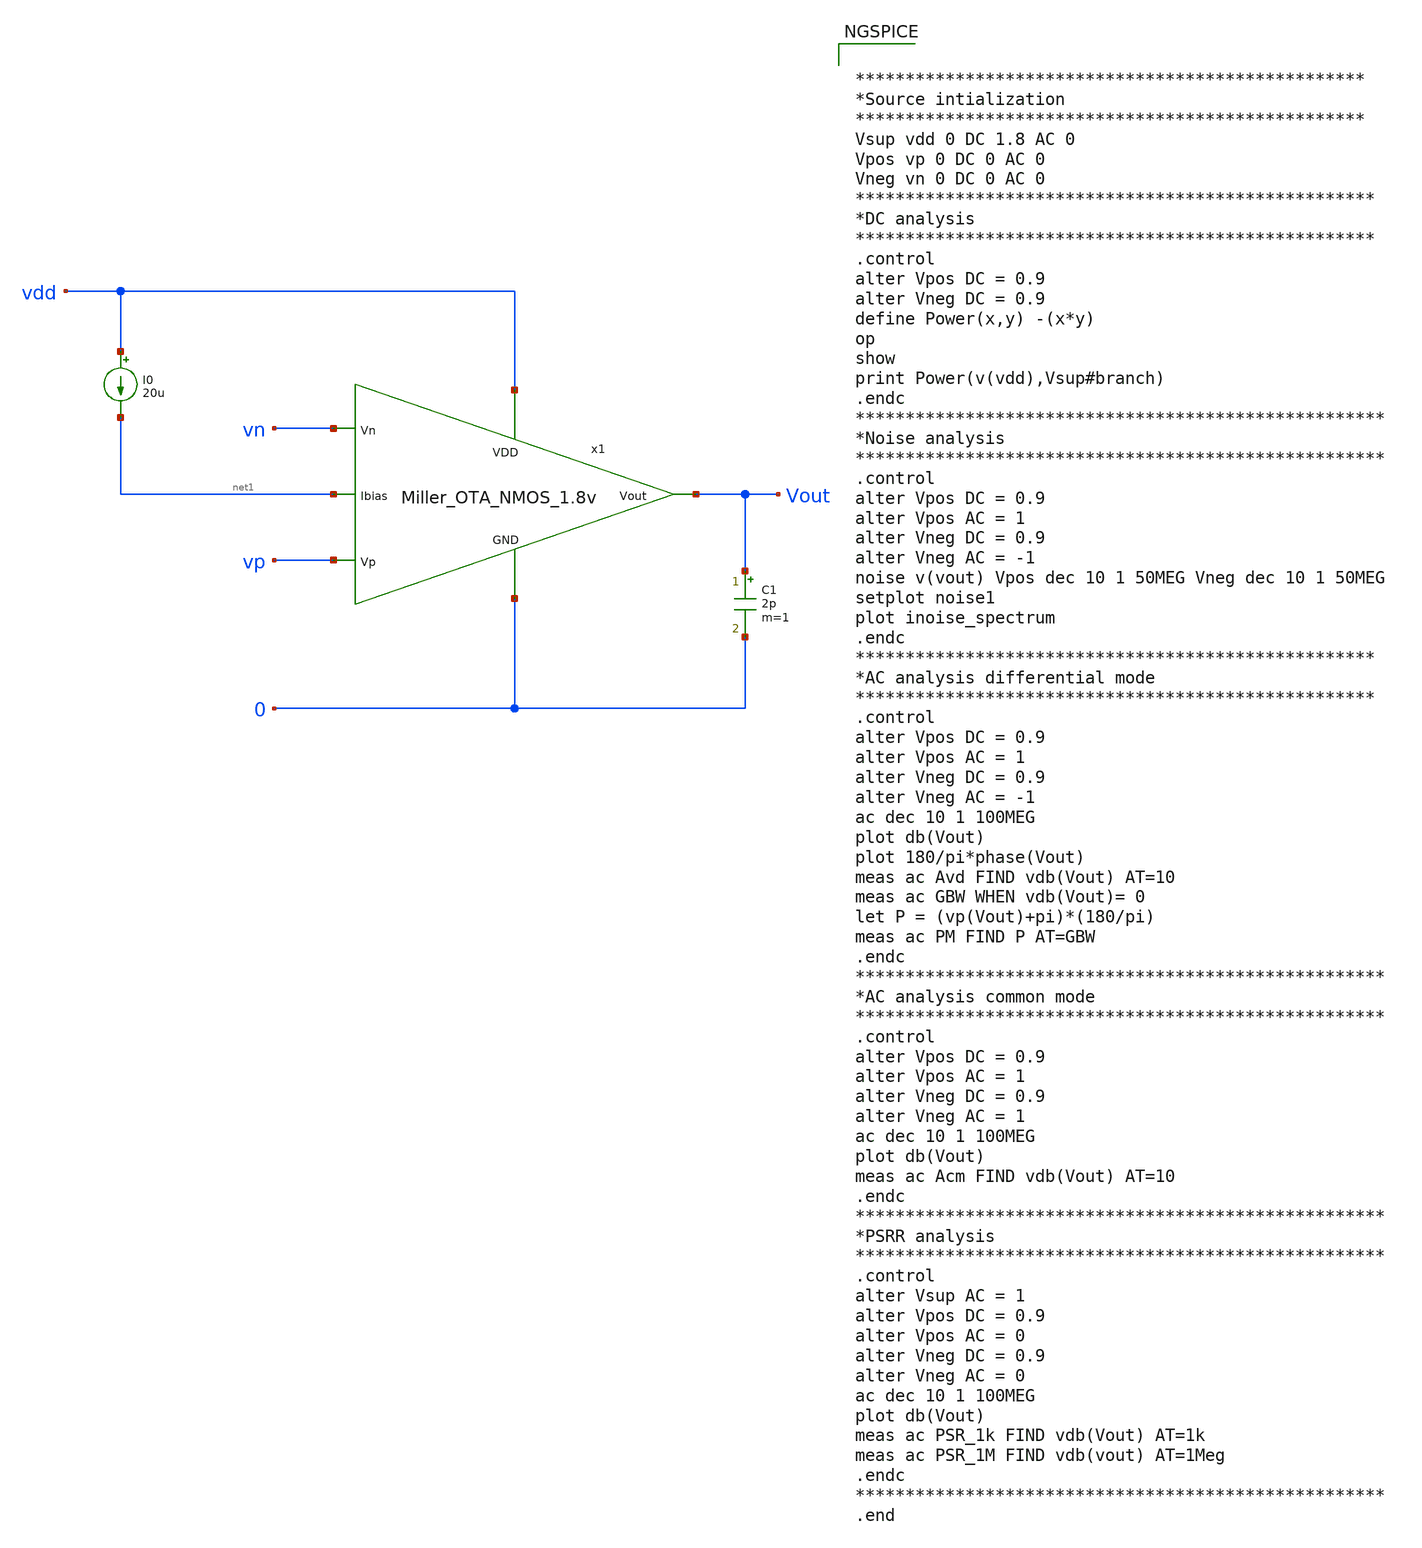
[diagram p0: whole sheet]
** sch_path: Analog_Blocks/OTA/Testbench/Miller_OTA_meas.sch
**.subckt Miller_OTA_meas
I0 vdd net1 20u
C1 Vout 0 2p m=1
x1 vdd vn vp Vout net1 0 Miller_OTA_NMOS_1.8v
**** begin user architecture code


***************************************************
*Source intialization
***************************************************
Vsup vdd 0 DC 1.8 AC 0
Vpos vp 0 DC 0 AC 0
Vneg vn 0 DC 0 AC 0
****************************************************
*DC analysis
****************************************************
.control
alter Vpos DC = 0.9
alter Vneg DC = 0.9
define Power(x,y) -(x*y)
op
show
print Power(v(vdd),Vsup#branch)
.endc
*****************************************************
*Noise analysis
*****************************************************
.control
alter Vpos DC = 0.9
alter Vpos AC = 1
alter Vneg DC = 0.9
alter Vneg AC = -1
noise v(vout) Vpos dec 10 1 50MEG Vneg dec 10 1 50MEG
setplot noise1
plot inoise_spectrum
.endc
****************************************************
*AC analysis differential mode
****************************************************
.control
alter Vpos DC = 0.9
alter Vpos AC = 1
alter Vneg DC = 0.9
alter Vneg AC = -1
ac dec 10 1 100MEG
plot db(Vout)
plot 180/pi*phase(Vout)
meas ac Avd FIND vdb(Vout) AT=10
meas ac GBW WHEN vdb(Vout)= 0
let P = (vp(Vout)+pi)*(180/pi)
meas ac PM FIND P AT=GBW
.endc
*****************************************************
*AC analysis common mode
*****************************************************
.control
alter Vpos DC = 0.9
alter Vpos AC = 1
alter Vneg DC = 0.9
alter Vneg AC = 1
ac dec 10 1 100MEG
plot db(Vout)
meas ac Acm FIND vdb(Vout) AT=10
.endc
*****************************************************
*PSRR analysis
*****************************************************
.control
alter Vsup AC = 1
alter Vpos DC = 0.9
alter Vpos AC = 0
alter Vneg DC = 0.9
alter Vneg AC = 0
ac dec 10 1 100MEG
plot db(Vout)
meas ac PSR_1k FIND vdb(Vout) AT=1k
meas ac PSR_1M FIND vdb(vout) AT=1Meg
.endc
*****************************************************
.end



.include $::SKYWATER_MODELS/cells/nfet_01v8/sky130_fd_pr__nfet_01v8__tt.corner.spice
.include $::SKYWATER_MODELS/cells/nfet_01v8_lvt/sky130_fd_pr__nfet_01v8_lvt__tt.corner.spice
.include $::SKYWATER_MODELS/cells/pfet_01v8/sky130_fd_pr__pfet_01v8__tt.corner.spice
.include $::SKYWATER_MODELS/cells/nfet_03v3_nvt/sky130_fd_pr__nfet_03v3_nvt__tt.corner.spice
.include $::SKYWATER_MODELS/cells/nfet_05v0_nvt/sky130_fd_pr__nfet_05v0_nvt__tt.corner.spice
.include $::SKYWATER_MODELS/cells/esd_nfet_01v8/sky130_fd_pr__esd_nfet_01v8__tt.corner.spice
.include $::SKYWATER_MODELS/cells/pfet_01v8_lvt/sky130_fd_pr__pfet_01v8_lvt__tt.corner.spice
.include $::SKYWATER_MODELS/cells/pfet_01v8_hvt/sky130_fd_pr__pfet_01v8_hvt__tt.corner.spice
.include $::SKYWATER_MODELS/cells/esd_pfet_g5v0d10v5/sky130_fd_pr__esd_pfet_g5v0d10v5__tt.corner.spice
.include $::SKYWATER_MODELS/cells/pfet_g5v0d10v5/sky130_fd_pr__pfet_g5v0d10v5__tt.corner.spice
.include $::SKYWATER_MODELS/cells/pfet_g5v0d16v0/sky130_fd_pr__pfet_g5v0d16v0__tt.corner.spice
.include $::SKYWATER_MODELS/cells/nfet_g5v0d10v5/sky130_fd_pr__nfet_g5v0d10v5__tt.corner.spice
.include $::SKYWATER_MODELS/cells/nfet_g5v0d16v0/sky130_fd_pr__nfet_g5v0d16v0__tt_discrete.corner.spice
.include $::SKYWATER_MODELS/cells/esd_nfet_g5v0d10v5/sky130_fd_pr__esd_nfet_g5v0d10v5__tt.corner.spice
.include $::SKYWATER_MODELS/models/corners/tt/nonfet.spice
* Mismatch parameters
.include $::SKYWATER_MODELS/cells/nfet_01v8/sky130_fd_pr__nfet_01v8__mismatch.corner.spice
.include $::SKYWATER_MODELS/cells/pfet_01v8/sky130_fd_pr__pfet_01v8__mismatch.corner.spice
.include $::SKYWATER_MODELS/cells/nfet_01v8_lvt/sky130_fd_pr__nfet_01v8_lvt__mismatch.corner.spice
.include $::SKYWATER_MODELS/cells/pfet_01v8_lvt/sky130_fd_pr__pfet_01v8_lvt__mismatch.corner.spice
.include $::SKYWATER_MODELS/cells/pfet_01v8_hvt/sky130_fd_pr__pfet_01v8_hvt__mismatch.corner.spice
.include $::SKYWATER_MODELS/cells/nfet_g5v0d10v5/sky130_fd_pr__nfet_g5v0d10v5__mismatch.corner.spice
.include $::SKYWATER_MODELS/cells/pfet_g5v0d10v5/sky130_fd_pr__pfet_g5v0d10v5__mismatch.corner.spice
.include $::SKYWATER_MODELS/cells/nfet_05v0_nvt/sky130_fd_pr__nfet_05v0_nvt__mismatch.corner.spice
.include $::SKYWATER_MODELS/cells/nfet_03v3_nvt/sky130_fd_pr__nfet_03v3_nvt__mismatch.corner.spice
* Resistor$::SKYWATER_MODELS/Capacitor
.include $::SKYWATER_MODELS/models/r+c/res_typical__cap_typical.spice
.include $::SKYWATER_MODELS/models/r+c/res_typical__cap_typical__lin.spice
* Special cells
.include $::SKYWATER_MODELS/models/corners/tt/specialized_cells.spice
* All models
.include $::SKYWATER_MODELS/models/all.spice
* Corner
.include $::SKYWATER_MODELS/models/corners/tt/rf.spice

**** end user architecture code
**.ends
.end
